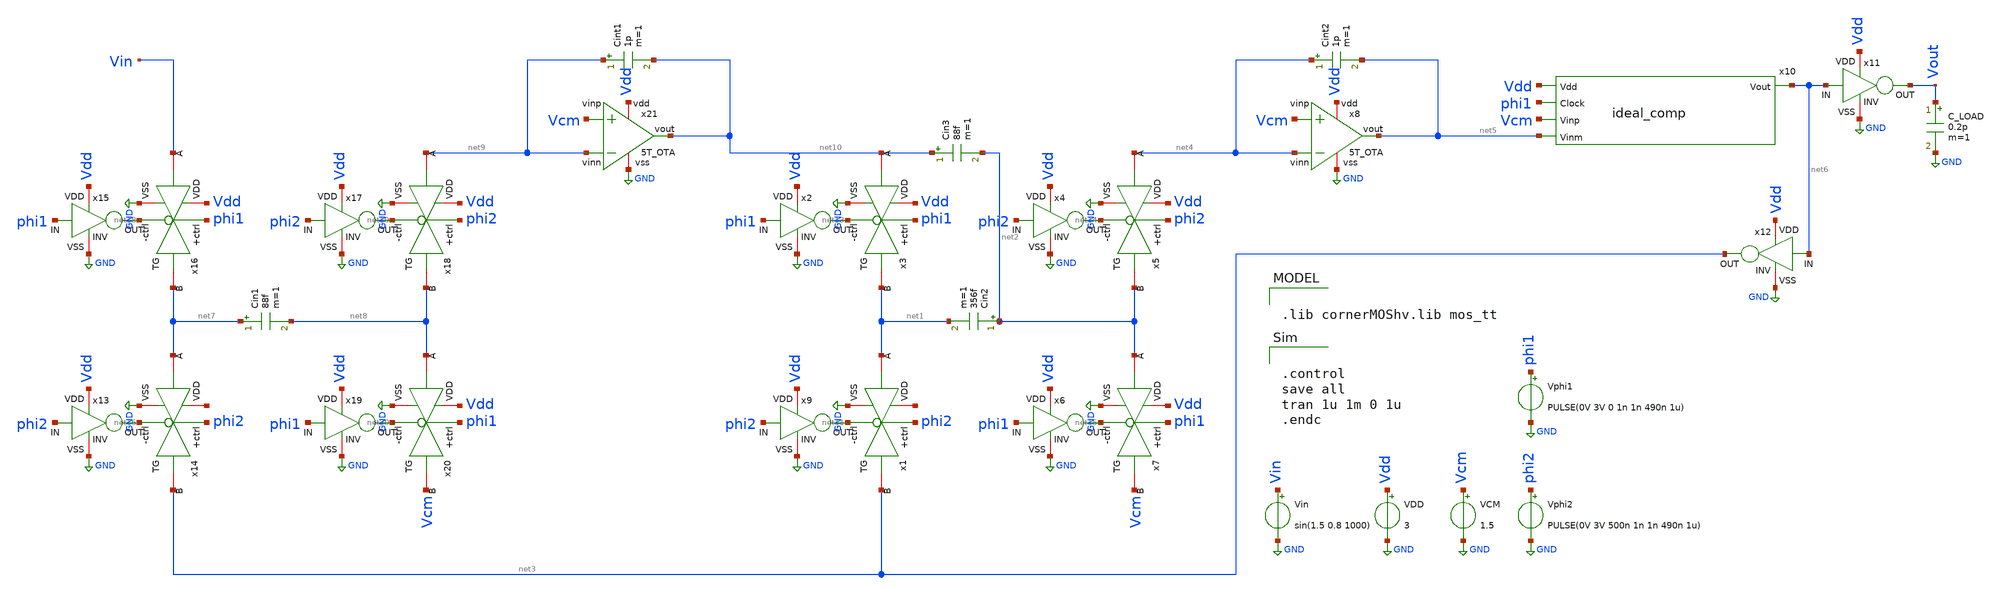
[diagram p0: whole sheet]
** sch_path: real_circuit/final/2nd_ord.sch
**.subckt 2nd_ord
C_LOAD Vout GND 0.2p m=1
x9 Vdd phi2 net11 GND INV
x1 phi2 net12 net3 net1 net11 GND TG
x2 Vdd phi1 net13 GND INV
x3 phi1 Vdd net1 net10 net13 GND TG
x4 Vdd phi2 net14 GND INV
x5 phi2 Vdd net2 net4 net14 GND TG
x6 Vdd phi1 net15 GND INV
x7 phi1 Vdd Vcm net2 net15 GND TG
Cint2 net4 net5 1p m=1
x8 Vdd net5 Vcm net4 GND 5T_OTA
VDD Vdd GND 3
VCM Vcm GND 1.5
Vin Vin GND sin(1.5 0.8 1000)
Vphi1 phi1 GND PULSE(0V 3V 0 1n 1n 490n 1u)
Vphi2 phi2 GND PULSE(0V 3V 500n 1n 1n 490n 1u)
x10 net6 Vdd phi1 Vcm net5 ideal_comp
x11 Vdd net6 Vout GND INV
x12 Vdd net6 net3 GND INV
x13 Vdd phi2 net16 GND INV
x14 phi2 net17 net3 net7 net16 GND TG
x15 Vdd phi1 net18 GND INV
x16 phi1 Vdd net7 Vin net18 GND TG
x17 Vdd phi2 net19 GND INV
x18 phi2 Vdd net8 net9 net19 GND TG
x19 Vdd phi1 net20 GND INV
x20 phi1 Vdd Vcm net8 net20 GND TG
Cin1 net7 net8 88f m=1
Cint1 net9 net10 1p m=1
x21 Vdd net10 Vcm net9 GND 5T_OTA
Cin2 net2 net1 356f m=1
Cin3 net10 net2 88f m=1
**** begin user architecture code


.control
save all
tran 1u 1m 0 1u
.endc



.lib cornerMOShv.lib mos_tt

**** end user architecture code
**.ends
.GLOBAL GND
.end
